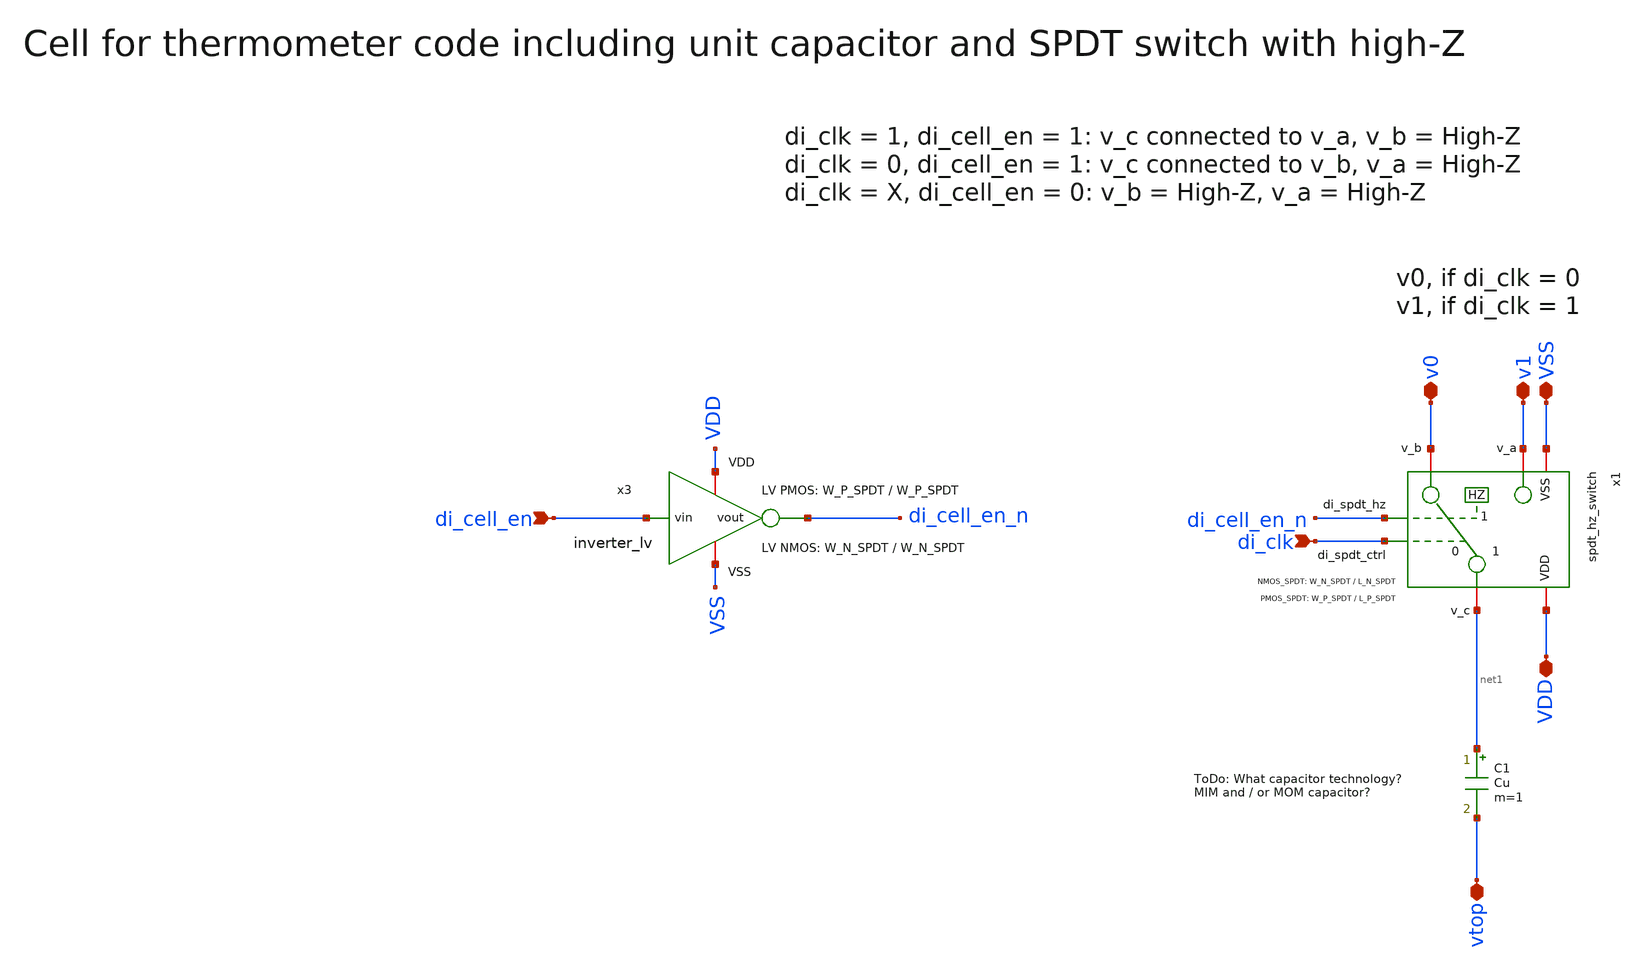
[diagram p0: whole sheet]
** sch_path: SG13G2_ATBS-ADC-main/xschem/dac/unit_cell.sch
**.subckt unit_cell di_cell_en VSS v0 VDD di_clk v1 vtop
*.ipin di_cell_en
*.iopin VSS
*.iopin v0
*.iopin VDD
*.ipin di_clk
*.iopin v1
*.iopin vtop
x1 VDD di_clk VSS net1 v0 v1 di_cell_en_n spdt_hz_switch W_P_TG=W_P_SPDT L_P_TG=L_P_SPDT
+ W_N_TG=W_N_SPDT L_N_TG=L_N_SPDT
C1 net1 vtop Cu m=1
x3 VDD di_cell_en di_cell_en_n VSS inverter_lv W_P=W_P_SPDT L_P=W_P_SPDT W_N=W_N_SPDT L_N=W_N_SPDT
**.ends

* expanding   symbol:  spdt_switch/spdt_hz_switch.sym # of pins=7
** sym_path: SG13G2_ATBS-ADC-main/xschem/spdt_switch/spdt_hz_switch.sym
** sch_path: SG13G2_ATBS-ADC-main/xschem/spdt_switch/spdt_hz_switch.sch
.subckt spdt_hz_switch VDD di_spdt_ctrl VSS v_c v_b v_a di_spdt_hz  W_P_TG=3.0u L_P_TG=0.13u
+ W_N_TG=1.0u L_N_TG=0.13u
*.iopin v_a
*.iopin v_b
*.iopin v_c
*.iopin VDD
*.iopin VSS
*.ipin di_spdt_ctrl
*.ipin di_spdt_hz
x1 VDD di_spdt_ctrl VSS net1 v_a di_spdt_ctrl_n transmission_gate_lv_wo_dummy W_P=W_P_TG L_P=L_P_TG
+ W_N=W_N_TG L_N=L_N_TG
x2 VDD di_spdt_ctrl_n VSS v_b net1 di_spdt_ctrl transmission_gate_lv_wo_dummy W_P=W_P_TG L_P=L_P_TG
+ W_N=W_N_TG L_N=L_N_TG
x8 VDD di_spdt_ctrl di_spdt_ctrl_n VSS inverter_lv W_P=W_P_TG L_P=L_P_TG W_N=W_N_TG L_N=L_N_TG
x3 VDD di_spdt_hz di_spdt_hz_n VSS inverter_lv W_P=W_P_TG L_P=L_P_TG W_N=W_N_TG L_N=L_N_TG
x4 VDD di_spdt_hz_n VSS v_c net1 di_spdt_hz transmission_gate_lv_wo_dummy W_P=W_P_TG L_P=L_P_TG
+ W_N=W_N_TG L_N=L_N_TG
.ends


* expanding   symbol:  inverter/inverter_lv.sym # of pins=4
** sym_path: SG13G2_ATBS-ADC-main/xschem/inverter/inverter_lv.sym
** sch_path: SG13G2_ATBS-ADC-main/xschem/inverter/inverter_lv.sch
.subckt inverter_lv VDD vin vout VSS  W_P=3.0u L_P=0.13u W_N=1.0u L_N=0.13u
*.ipin vin
*.iopin VDD
*.iopin VSS
*.opin vout
XM1 vout vin VDD VDD sg13_lv_pmos w=W_P l=L_P ng=1 m=1 mm_ok=1
XM2 vout vin VSS VSS sg13_lv_nmos w=W_N l=L_N ng=1 m=1 mm_ok=1
.ends


* expanding   symbol:  transmission_gate/transmission_gate_lv_wo_dummy.sym # of pins=6
** sym_path: SG13G2_ATBS-ADC-main/xschem/transmission_gate/transmission_gate_lv_wo_dummy.sym
** sch_path: SG13G2_ATBS-ADC-main/xschem/transmission_gate/transmission_gate_lv_wo_dummy.sch
.subckt transmission_gate_lv_wo_dummy VDD di_tg_ctrl VSS v_b v_a di_tg_ctrl_n  W_P=1.0u L_P=0.13u
+ W_N=1.0u L_N=0.13u
*.iopin v_a
*.iopin v_b
*.iopin VDD
*.iopin VSS
*.ipin di_tg_ctrl
*.ipin di_tg_ctrl_n
XM1 v_a di_tg_ctrl v_b VSS sg13_lv_nmos w=W_N l=L_N ng=1 m=1 mm_ok=1
XM2 v_a di_tg_ctrl_n v_b VDD sg13_lv_pmos w=W_P l=L_P ng=1 m=1 mm_ok=1
.ends

.end
